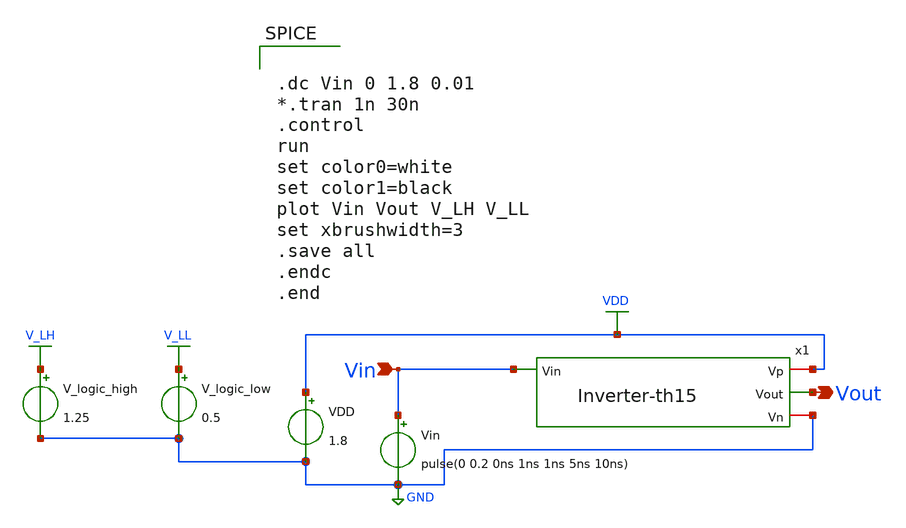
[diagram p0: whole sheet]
** sch_path: xschem/Vth_sch/Pre_layout/Inverter-th15.sch
**.subckt Inverter-th15 Vin Vout
*.ipin Vin
*.opin Vout
VDD VDD GND 1.8
Vin Vin GND pulse(0 0.2 0ns 1ns 1ns 5ns 10ns)
V_logic_high V_LH GND 1.25
V_logic_low V_LL GND 0.5
x1 VDD Vout Vin GND Inverter-th15
**** begin user architecture code


.lib /usr/local/share/pdk/sky130A/libs.tech/ngspice/sky130.lib.spice tt

.save all





.dc Vin 0 1.8 0.01
*.tran 1n 30n
.control
run
set color0=white
set color1=black
plot Vin Vout V_LH V_LL
set xbrushwidth=3
.save all
.endc
.end


**** end user architecture code
**.ends

* expanding   symbol:  /home/exotic/Desktop/ASIC_ADC/xschem/Vth_sch/Symbol/Inverter-th15.sym # of
*+ pins=4
** sym_path: xschem/Vth_sch/Symbol/Inverter-th15.sym
** sch_path: xschem/Vth_sch/Symbol/Inverter-th15.sch
.subckt Inverter-th15 Vp Vout Vin Vn
*.ipin Vin
*.opin Vout
*.iopin Vn
*.iopin Vp
XM1 Vout Vin Vp Vp sky130_fd_pr__pfet_01v8 L=0.15 W=30 nf=1 ad='int((nf+1)/2) * W/nf * 0.29' as='int((nf+2)/2) * W/nf * 0.29'
+ pd='2*int((nf+1)/2) * (W/nf + 0.29)' ps='2*int((nf+2)/2) * (W/nf + 0.29)' nrd='0.29 / W' nrs='0.29 / W'
+ sa=0 sb=0 sd=0 mult=1 m=1
XM3 net1 Vin net2 net2 sky130_fd_pr__nfet_01v8 L=35 W=0.36 nf=1 ad='int((nf+1)/2) * W/nf * 0.29' as='int((nf+2)/2) * W/nf * 0.29'
+ pd='2*int((nf+1)/2) * (W/nf + 0.29)' ps='2*int((nf+2)/2) * (W/nf + 0.29)' nrd='0.29 / W' nrs='0.29 / W'
+ sa=0 sb=0 sd=0 mult=1 m=1
XM4 Vout Vin net1 net1 sky130_fd_pr__nfet_01v8 L=35 W=0.36 nf=1 ad='int((nf+1)/2) * W/nf * 0.29' as='int((nf+2)/2) * W/nf * 0.29'
+ pd='2*int((nf+1)/2) * (W/nf + 0.29)' ps='2*int((nf+2)/2) * (W/nf + 0.29)' nrd='0.29 / W' nrs='0.29 / W'
+ sa=0 sb=0 sd=0 mult=1 m=1
XM5 Vout Vin Vp Vp sky130_fd_pr__pfet_01v8 L=0.15 W=30 nf=1 ad='int((nf+1)/2) * W/nf * 0.29' as='int((nf+2)/2) * W/nf * 0.29'
+ pd='2*int((nf+1)/2) * (W/nf + 0.29)' ps='2*int((nf+2)/2) * (W/nf + 0.29)' nrd='0.29 / W' nrs='0.29 / W'
+ sa=0 sb=0 sd=0 mult=1 m=1
XM6 Vout Vin Vp Vp sky130_fd_pr__pfet_01v8 L=0.15 W=30 nf=1 ad='int((nf+1)/2) * W/nf * 0.29' as='int((nf+2)/2) * W/nf * 0.29'
+ pd='2*int((nf+1)/2) * (W/nf + 0.29)' ps='2*int((nf+2)/2) * (W/nf + 0.29)' nrd='0.29 / W' nrs='0.29 / W'
+ sa=0 sb=0 sd=0 mult=1 m=1
XM2 Vn Vn net2 net2 sky130_fd_pr__pfet_01v8 L=0.15 W=1 nf=1 ad='int((nf+1)/2) * W/nf * 0.29' as='int((nf+2)/2) * W/nf * 0.29'
+ pd='2*int((nf+1)/2) * (W/nf + 0.29)' ps='2*int((nf+2)/2) * (W/nf + 0.29)' nrd='0.29 / W' nrs='0.29 / W'
+ sa=0 sb=0 sd=0 mult=1 m=1
.ends

.GLOBAL VDD
.GLOBAL GND
.GLOBAL V_LH
.GLOBAL V_LL
.end
